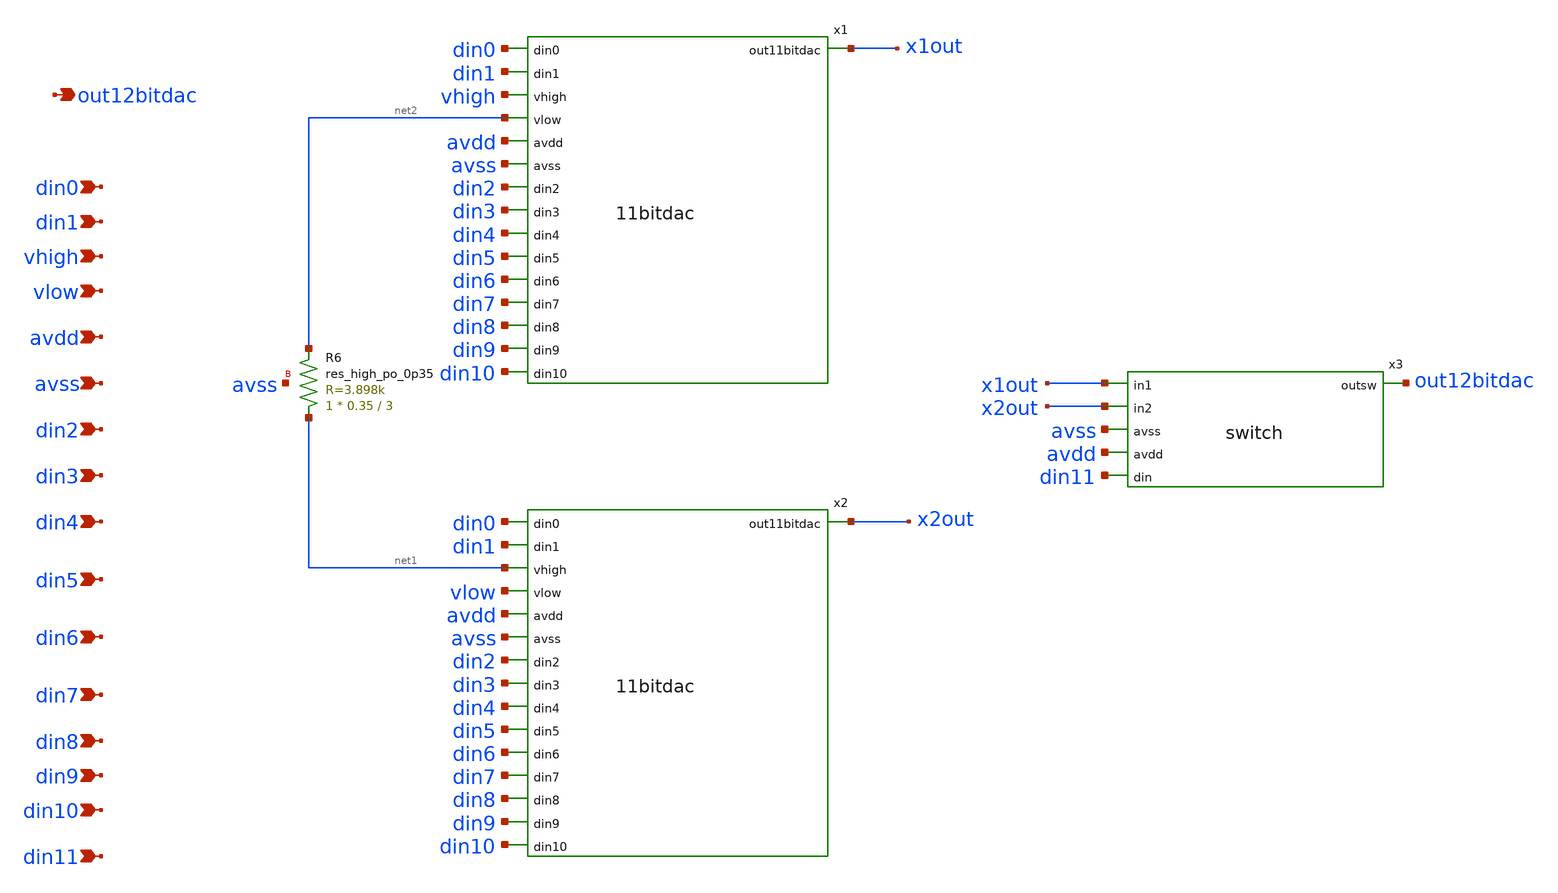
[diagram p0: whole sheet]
** sch_path: xschem/12bitdac.sch
**.subckt 12bitdac din0 din1 vhigh vlow avdd avss din2 din3 out12bitdac din4 din5 din6 din7 din8
*+ din9 din10 din11
*.ipin din0
*.ipin din1
*.ipin vhigh
*.ipin vlow
*.ipin avdd
*.ipin avss
*.ipin din2
*.ipin din3
*.opin out12bitdac
*.ipin din4
*.ipin din5
*.ipin din6
*.ipin din7
*.ipin din8
*.ipin din9
*.ipin din10
*.ipin din11
x1 x1out din0 din1 vhigh net2 avdd avss din2 din3 din4 din5 din6 din7 din8 din9 din10 11bitdac
x2 x2out din0 din1 net1 vlow avdd avss din2 din3 din4 din5 din6 din7 din8 din9 din10 11bitdac
XR6 net1 net2 avss sky130_fd_pr__res_high_po_0p35 L=3 mult=1 m=1
x3 out12bitdac x1out x2out avss avdd din11 switch
**.ends
.end
